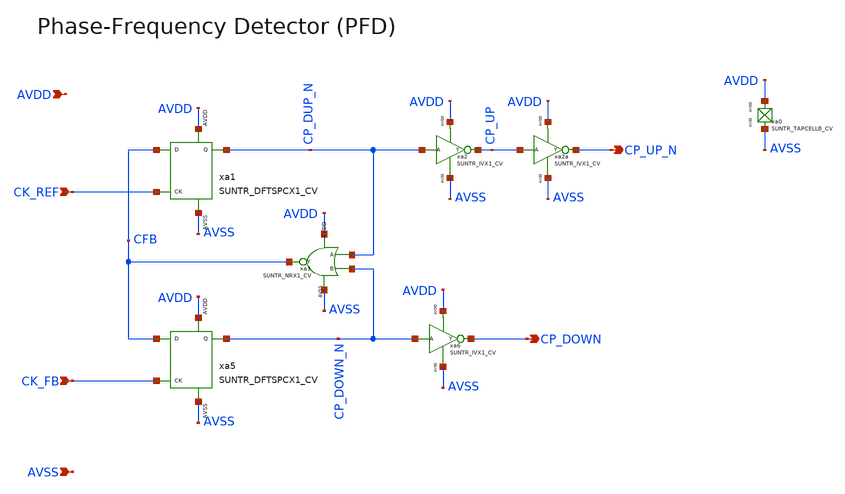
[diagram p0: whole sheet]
** sch_path: design/SUN_PLL_SKY130NM/SUN_PLL_PFD.sch
**.subckt SUN_PLL_PFD AVDD CP_UP_N CK_REF CP_DOWN CK_FB AVSS
*.ipin AVDD
*.opin CP_UP_N
*.ipin CK_REF
*.opin CP_DOWN
*.ipin CK_FB
*.ipin AVSS
xa3 CP_DUP_N CP_DOWN_N CFB AVDD AVSS SUNTR_NRX1_CV
xa2 CP_DUP_N CP_UP AVDD AVSS SUNTR_IVX1_CV
xa6 CP_DOWN_N CP_DOWN AVDD AVSS SUNTR_IVX1_CV
xa1 CFB CK_REF CP_DUP_N AVDD AVSS SUNTR_DFTSPCX1_CV xoffset=0 yoffset=0 angle=0
xa5 CFB CK_FB CP_DOWN_N AVDD AVSS SUNTR_DFTSPCX1_CV xoffset=0 yoffset=0 angle=0
xa0 AVDD AVSS SUNTR_TAPCELLB_CV xoffset=0 yoffset=0 angle=0
xa2a CP_UP CP_UP_N AVDD AVSS SUNTR_IVX1_CV
**.ends
.end
